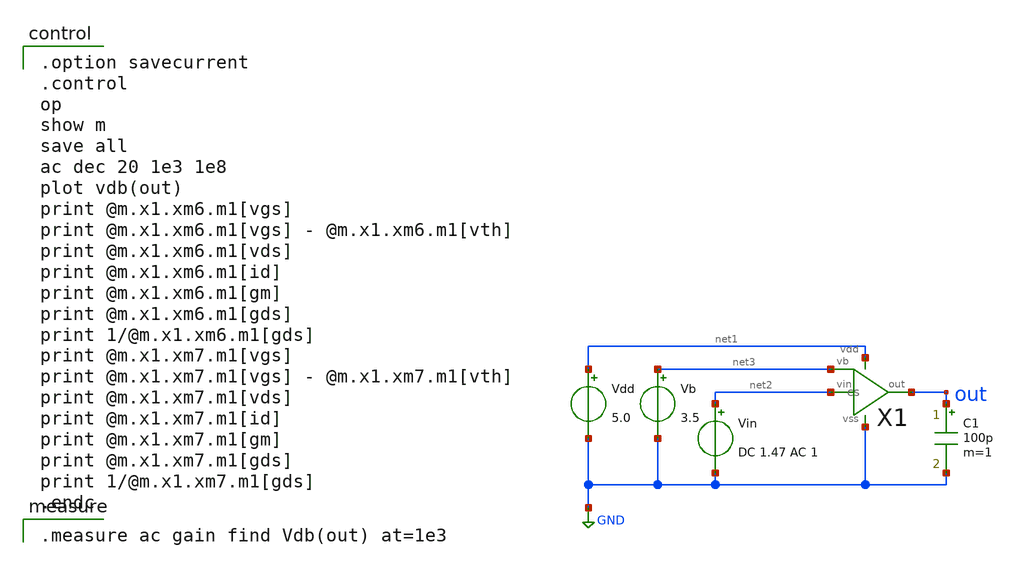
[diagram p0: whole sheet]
** sch_path: schematic/20250924_OSS_Workshop/ishikai/opamp/sample/cs_ac.sch
**.subckt cs_ac
Vdd net1 GND 5.0
Vb net3 GND 3.5
Vin net2 GND DC 1.47 AC 1
X1 net2 net3 out net1 GND cs
C1 out GND 100p m=1
**** begin user architecture code

.option savecurrent
.control
op
show m
save all
ac dec 20 1e3 1e8
plot vdb(out)
print @m.x1.xm6.m1[vgs]
print @m.x1.xm6.m1[vgs] - @m.x1.xm6.m1[vth]
print @m.x1.xm6.m1[vds]
print @m.x1.xm6.m1[id]
print @m.x1.xm6.m1[gm]
print @m.x1.xm6.m1[gds]
print 1/@m.x1.xm6.m1[gds]
print @m.x1.xm7.m1[vgs]
print @m.x1.xm7.m1[vgs] - @m.x1.xm7.m1[vth]
print @m.x1.xm7.m1[vds]
print @m.x1.xm7.m1[id]
print @m.x1.xm7.m1[gm]
print @m.x1.xm7.m1[gds]
print 1/@m.x1.xm7.m1[gds]
.endc


.measure ac gain find Vdb(out) at=1e3

 .include $::LIB/../ip62_models
**** end user architecture code
**.ends

* expanding   symbol:  cs.sym # of pins=5
** sym_path: schematic/20250924_OSS_Workshop/ishikai/opamp/sample/cs.sym
** sch_path: schematic/20250924_OSS_Workshop/ishikai/opamp/sample/cs.sch
.subckt cs vin vb out vdd vss
*.ipin vb
*.ipin vin
*.opin out
*.iopin vss
*.iopin vdd
XM6 out vb vdd vdd PMOS w=270u l=1u as=0 ad=0 ps=0 pd=0 nrd=0 nrs=0 m=1
XM7 out vin vss vss NMOS w=90u l=1u as=0 ad=0 ps=0 pd=0 nrd=0 nrs=0 m=1
.ends

.GLOBAL GND
.end
